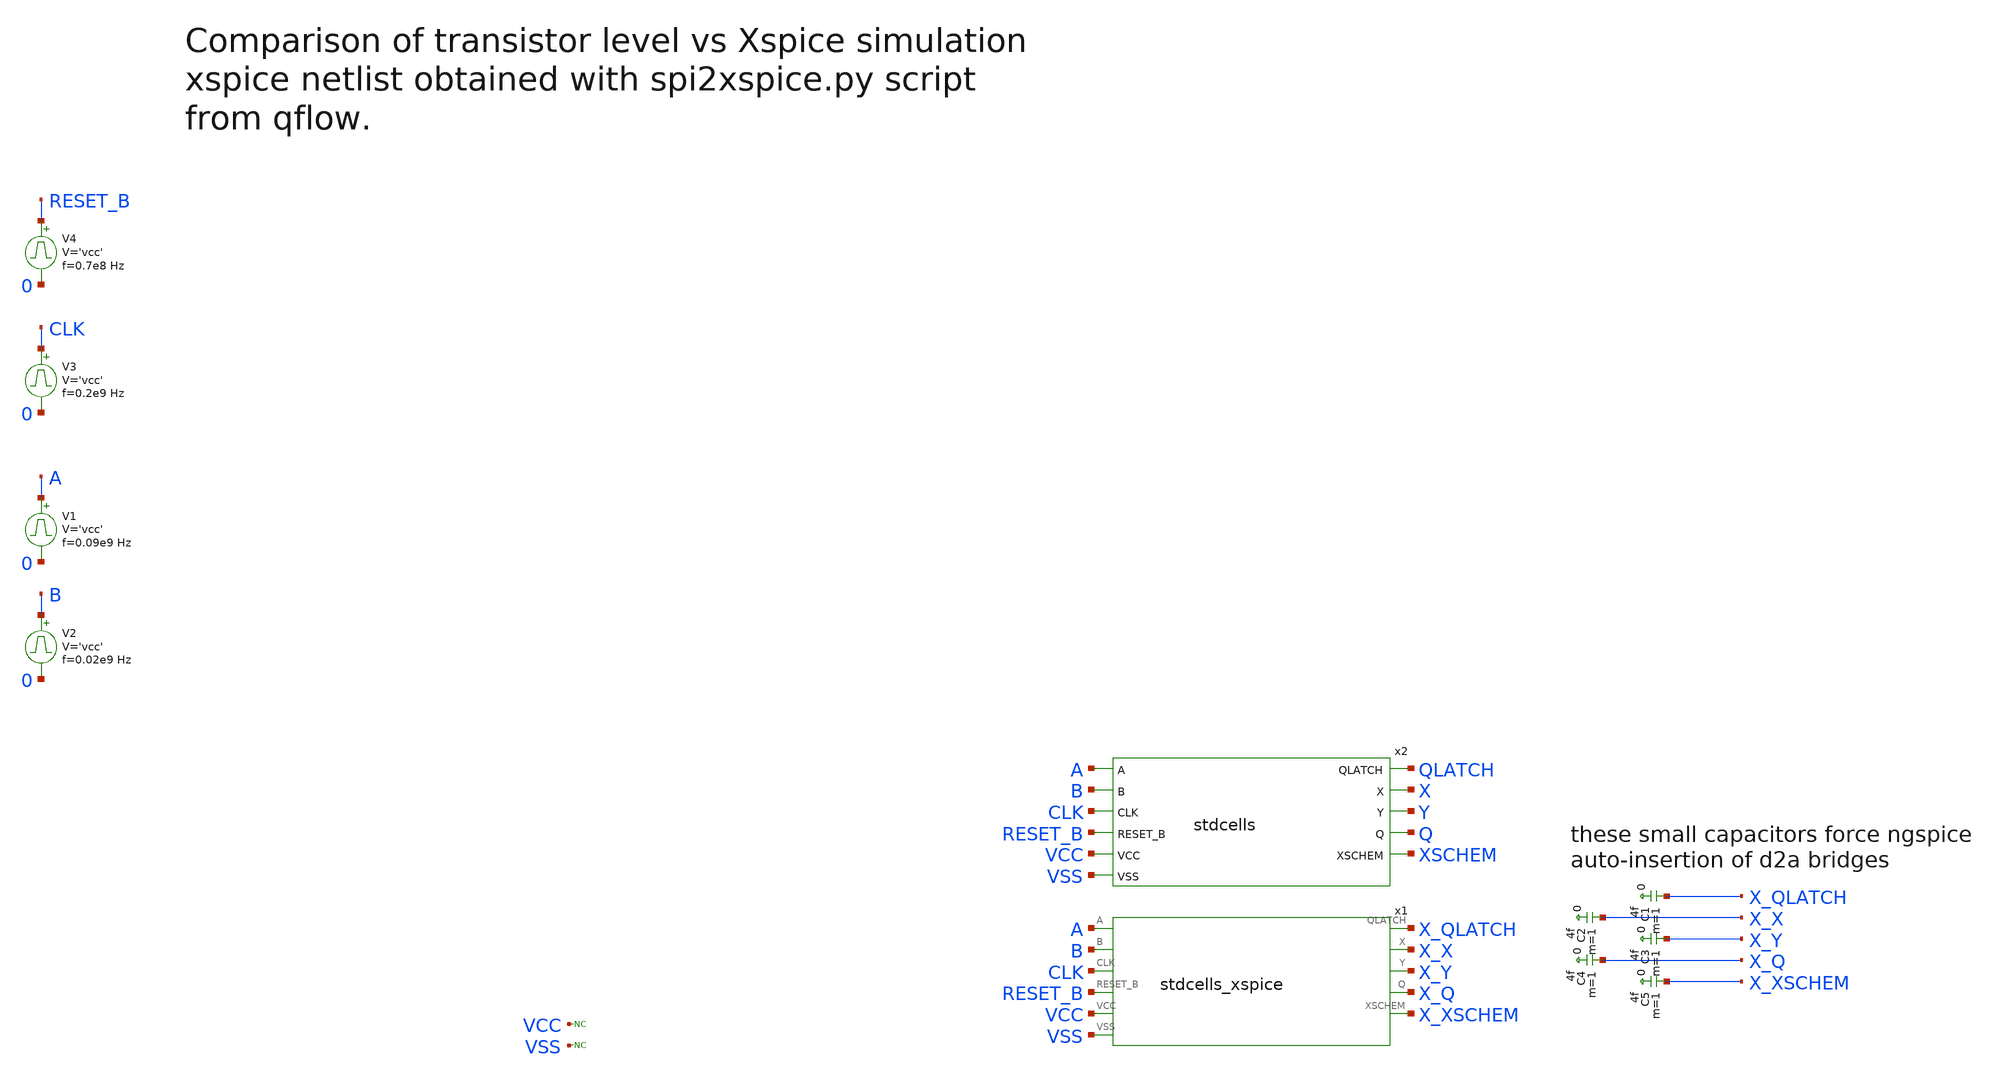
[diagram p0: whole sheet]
** sch_path: sky130A/xschem_libs/sky130_tests_ase/test_stdcells/schematic/test_stdcells.sch
* Copyright 2021 Stefan Frederik Schippers
* Licensed under the Apache License, Version 2.0 (the "License");
* you may not use this file except in compliance with the License.
* You may obtain a copy of the License at
* https://www.apache.org/licenses/LICENSE-2.0
* Unless required by applicable law or agreed to in writing, software
* distributed under the License is distributed on an "AS IS" BASIS,
* WITHOUT WARRANTIES OR CONDITIONS OF ANY KIND, either express or implied.
* See the License for the specific language governing permissions and
* limitations under the License.
**.subckt test_stdcells
V1 A 0 pulse 0 'vcc' '0.495/ 0.09e9 ' '0.01/0.09e9 ' '0.01/0.09e9 ' '0.49/0.09e9 ' '1/0.09e9 '
V2 B 0 pulse 0 'vcc' '0.495/ 0.02e9 ' '0.01/0.02e9 ' '0.01/0.02e9 ' '0.49/0.02e9 ' '1/0.02e9 '
V3 CLK 0 pulse 0 'vcc' '0.495/ 0.2e9 ' '0.01/0.2e9 ' '0.01/0.2e9 ' '0.49/0.2e9 ' '1/0.2e9 '
V4 RESET_B 0 pulse 0 'vcc' '0.495/ 0.7e8 ' '0.01/0.7e8 ' '0.01/0.7e8 ' '0.49/0.7e8 ' '1/0.7e8 '
x2 QLATCH A X B Y CLK Q RESET_B XSCHEM VCC VSS stdcells
x1 X_QLATCH A X_X B X_Y CLK X_Q RESET_B X_XSCHEM VCC VSS stdcells_xspice
* noconn VCC
* noconn VSS
C1 X_QLATCH 0 4f m=1
C2 X_X 0 4f m=1
C3 X_Y 0 4f m=1
C4 X_Q 0 4f m=1
C5 X_XSCHEM 0 4f m=1
**** begin user architecture code


.model ddflop d_dff(ic=0 rise_delay=200p fall_delay=200p clk_delay=20p reset_delay=20p data_load=10f
+ reset_load=10f clk_load=10f)
.model dlatch d_dlatch(ic=0 rise_delay=200p fall_delay=200p data_delay = 20p enable_delay=20p
+ reset_delay=200p data_load=10f reset_load=10f enable_load=10f)
.model dzero d_pulldown(load=10f)
.model done d_pullup(load=10f)
.model d_lut_sky130_fd_sc_hd__nand2_1 d_lut (rise_delay=200p fall_delay=200p input_load=10f
+ table_values "1110")
.model d_lut_sky130_fd_sc_hd__nor2b_1 d_lut (rise_delay=200p fall_delay=200p input_load=10f
+ table_values "0010")
.model d_lut_sky130_fd_sc_hd__a31o_2 d_lut (rise_delay=200p fall_delay=200p input_load=10f
+ table_values "0000000111111111")
.model d_lut_sky130_fd_sc_hd__inv_2 d_lut (rise_delay=200p fall_delay=200p input_load=10f
+ table_values "10")
.model d_lut_sky130_fd_sc_hd__buf_2 d_lut (rise_delay=200p fall_delay=200p input_load=10f
+ table_values "01")




vvcc vcc 0 dc 'vcc'
vvss vss 0 0


**** end user architecture code
**.ends
.end
